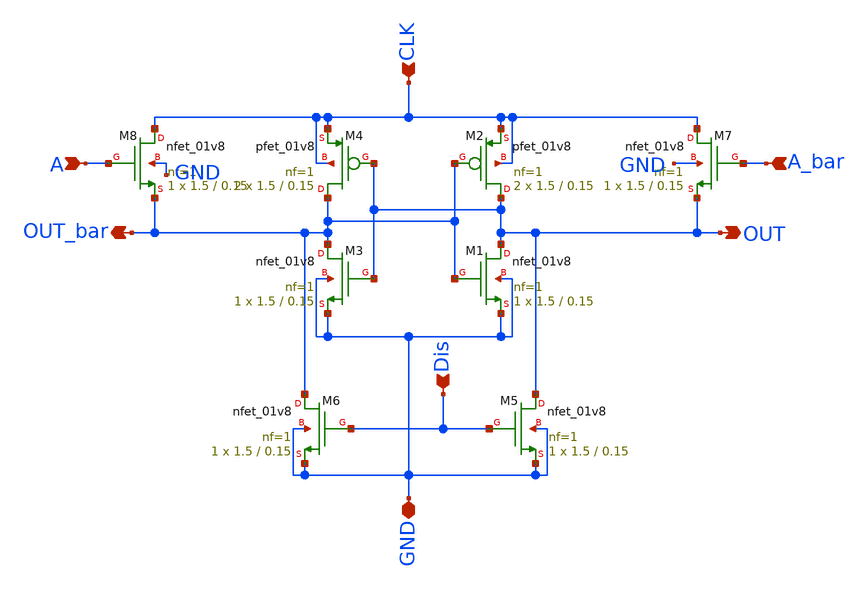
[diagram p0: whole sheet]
** sch_path: skywater_stuff/EESPFAL_INV4_magic_checked.sch
**.subckt EESPFAL_INV4_magic_checked A A_bar OUT OUT_bar Dis GND CLK
*.ipin A
*.ipin A_bar
*.opin OUT
*.opin OUT_bar
*.ipin Dis
*.iopin GND
*.ipin CLK
XM7 CLK A_bar OUT GND sky130_fd_pr__nfet_01v8 L=0.15 W=1.5 nf=1 ad='int((nf+1)/2) * W/nf * 0.29' as='int((nf+2)/2) * W/nf * 0.29'
+ pd='2*int((nf+1)/2) * (W/nf + 0.29)' ps='2*int((nf+2)/2) * (W/nf + 0.29)' nrd='0.29 / W' nrs='0.29 / W'
+ sa=0 sb=0 sd=0 mult=1 m=1
XM3 OUT_bar OUT GND GND sky130_fd_pr__nfet_01v8 L=0.15 W=1.5 nf=1 ad='int((nf+1)/2) * W/nf * 0.29' as='int((nf+2)/2) * W/nf * 0.29'
+ pd='2*int((nf+1)/2) * (W/nf + 0.29)' ps='2*int((nf+2)/2) * (W/nf + 0.29)' nrd='0.29 / W' nrs='0.29 / W'
+ sa=0 sb=0 sd=0 mult=1 m=1
XM5 OUT Dis GND GND sky130_fd_pr__nfet_01v8 L=0.15 W=1.5 nf=1 ad='int((nf+1)/2) * W/nf * 0.29' as='int((nf+2)/2) * W/nf * 0.29'
+ pd='2*int((nf+1)/2) * (W/nf + 0.29)' ps='2*int((nf+2)/2) * (W/nf + 0.29)' nrd='0.29 / W' nrs='0.29 / W'
+ sa=0 sb=0 sd=0 mult=1 m=1
XM6 OUT_bar Dis GND GND sky130_fd_pr__nfet_01v8 L=0.15 W=1.5 nf=1 ad='int((nf+1)/2) * W/nf * 0.29' as='int((nf+2)/2) * W/nf * 0.29'
+ pd='2*int((nf+1)/2) * (W/nf + 0.29)' ps='2*int((nf+2)/2) * (W/nf + 0.29)' nrd='0.29 / W' nrs='0.29 / W'
+ sa=0 sb=0 sd=0 mult=1 m=1
XM8 CLK A OUT_bar GND sky130_fd_pr__nfet_01v8 L=0.15 W=1.5 nf=1 ad='int((nf+1)/2) * W/nf * 0.29' as='int((nf+2)/2) * W/nf * 0.29'
+ pd='2*int((nf+1)/2) * (W/nf + 0.29)' ps='2*int((nf+2)/2) * (W/nf + 0.29)' nrd='0.29 / W' nrs='0.29 / W'
+ sa=0 sb=0 sd=0 mult=1 m=1
XM2 OUT OUT_bar CLK CLK sky130_fd_pr__pfet_01v8 L=0.15 W=1.5 nf=1 ad='int((nf+1)/2) * W/nf * 0.29' as='int((nf+2)/2) * W/nf * 0.29'
+ pd='2*int((nf+1)/2) * (W/nf + 0.29)' ps='2*int((nf+2)/2) * (W/nf + 0.29)' nrd='0.29 / W' nrs='0.29 / W'
+ sa=0 sb=0 sd=0 mult=2 m=2
XM1 OUT OUT_bar GND GND sky130_fd_pr__nfet_01v8 L=0.15 W=1.5 nf=1 ad='int((nf+1)/2) * W/nf * 0.29' as='int((nf+2)/2) * W/nf * 0.29'
+ pd='2*int((nf+1)/2) * (W/nf + 0.29)' ps='2*int((nf+2)/2) * (W/nf + 0.29)' nrd='0.29 / W' nrs='0.29 / W'
+ sa=0 sb=0 sd=0 mult=1 m=1
XM4 OUT_bar OUT CLK CLK sky130_fd_pr__pfet_01v8 L=0.15 W=1.5 nf=1 ad='int((nf+1)/2) * W/nf * 0.29' as='int((nf+2)/2) * W/nf * 0.29'
+ pd='2*int((nf+1)/2) * (W/nf + 0.29)' ps='2*int((nf+2)/2) * (W/nf + 0.29)' nrd='0.29 / W' nrs='0.29 / W'
+ sa=0 sb=0 sd=0 mult=2 m=2
**.ends
.end
